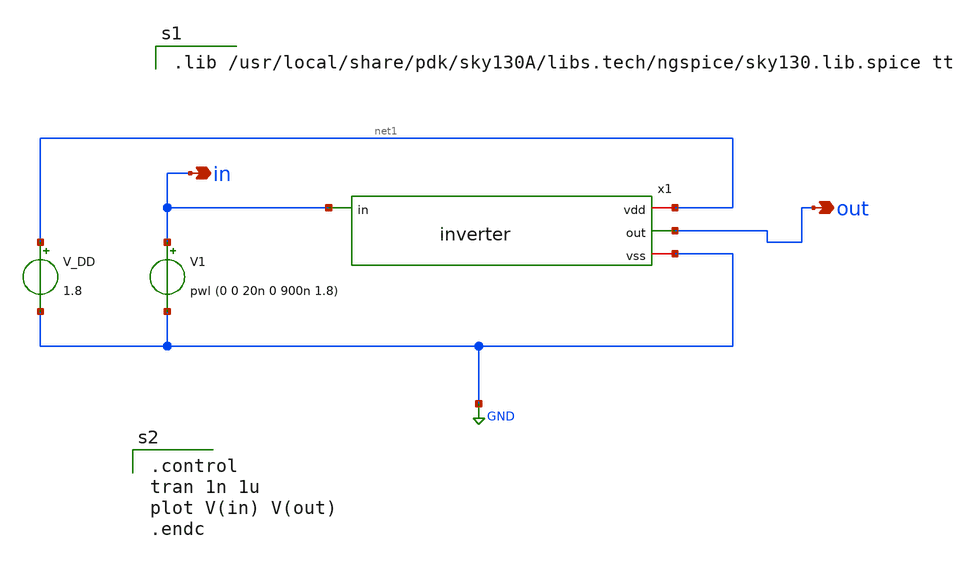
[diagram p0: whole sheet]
** sch_path: inverter/xschem/inverter_tb.sch
**.subckt inverter_tb out in
*.opin out
*.opin in
x1 net1 in out GND inverter
V1 in GND pwl (0 0 20n 0 900n 1.8)
V_DD net1 GND 1.8
**** begin user architecture code

.lib /usr/local/share/pdk/sky130A/libs.tech/ngspice/sky130.lib.spice tt


.control
tran 1n 1u
plot V(in) V(out)
.endc

**** end user architecture code
**.ends

* expanding   symbol:  inverter.sym # of pins=4
** sym_path: inverter/xschem/inverter.sym
** sch_path: inverter/xschem/inverter.sch
.subckt inverter vdd in out vss
*.ipin in
*.opin out
*.iopin vdd
*.iopin vss
XM2 out in vdd vdd sky130_fd_pr__pfet_01v8 L=0.18 W=3 nf=3 ad='int((nf+1)/2) * W/nf * 0.29' as='int((nf+2)/2) * W/nf * 0.29'
+ pd='2*int((nf+1)/2) * (W/nf + 0.29)' ps='2*int((nf+2)/2) * (W/nf + 0.29)' nrd='0.29 / W' nrs='0.29 / W'
+ sa=0 sb=0 sd=0 mult=1 m=1
XM1 out in vss vss sky130_fd_pr__nfet_01v8 L=0.2 W=4.5 nf=1 ad='int((nf+1)/2) * W/nf * 0.29' as='int((nf+2)/2) * W/nf * 0.29'
+ pd='2*int((nf+1)/2) * (W/nf + 0.29)' ps='2*int((nf+2)/2) * (W/nf + 0.29)' nrd='0.29 / W' nrs='0.29 / W'
+ sa=0 sb=0 sd=0 mult=1 m=1
.ends

.GLOBAL GND
.end
